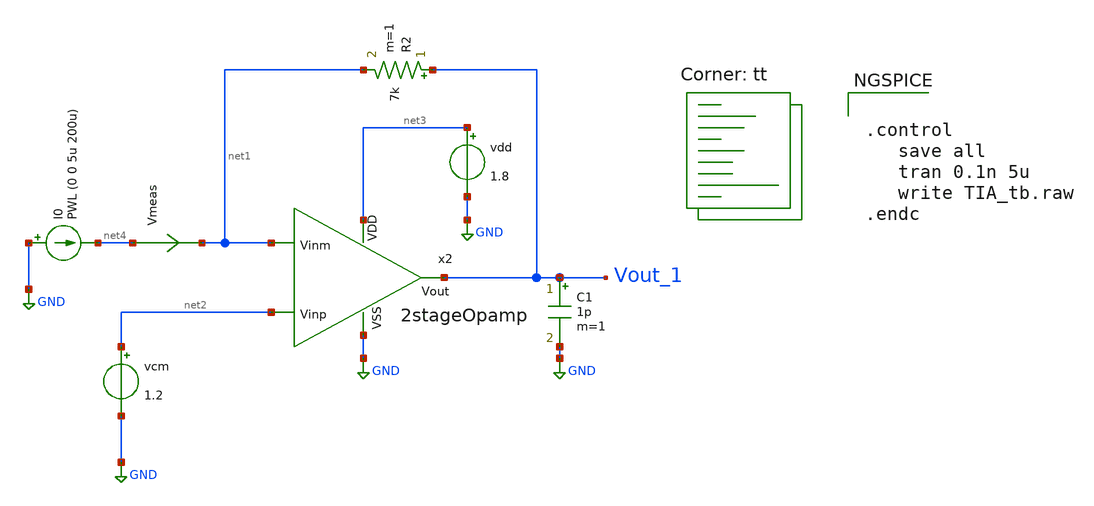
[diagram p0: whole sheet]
** sch_path: xschem/test/xschem/dec24_2stage_tbs/TIA_tb.sch
**.subckt TIA_tb
x2 net3 net1 net2 Vout_1 GND 2stageOpamp
vdd net3 GND 1.8
C1 Vout_1 GND 1p m=1
R2 Vout_1 net1 7k m=1
I0 GND net4 PWL (0 0 5u 200u)
Vmeas net4 net1 0
.save i(vmeas)
vcm net2 GND 1.2
**** begin user architecture code
.lib $::SKYWATER_MODELS/sky130.lib.spice tt


.control
   save all
   tran 0.1n 5u
   write TIA_tb.raw
.endc


**** end user architecture code
**.ends

* expanding   symbol:  amplifiers/dec24/2stageOpamp.sym # of pins=5
** sym_path: amplifiers/dec24/2stageOpamp.sym
** sch_path: amplifiers/dec24/2stageOpamp.sch
.subckt 2stageOpamp VDD Vinm Vinp Vout VSS
*.ipin Vinm
*.ipin Vinp
*.opin Vout
*.ipin VSS
*.ipin VDD
XM8 Vout net1 VSS VSS sky130_fd_pr__nfet_01v8 L=1 W=6 nf=1 ad='int((nf+1)/2) * W/nf * 0.29' as='int((nf+2)/2) * W/nf * 0.29'
+ pd='2*int((nf+1)/2) * (W/nf + 0.29)' ps='2*int((nf+2)/2) * (W/nf + 0.29)' nrd='0.29 / W' nrs='0.29 / W'
+ sa=0 sb=0 sd=0 mult=8 m=8
XM2 Vout Vb1 VDD VDD sky130_fd_pr__pfet_01v8_lvt L=1 W=9 nf=1 ad='int((nf+1)/2) * W/nf * 0.29' as='int((nf+2)/2) * W/nf * 0.29'
+ pd='2*int((nf+1)/2) * (W/nf + 0.29)' ps='2*int((nf+2)/2) * (W/nf + 0.29)' nrd='0.29 / W' nrs='0.29 / W'
+ sa=0 sb=0 sd=0 mult=3 m=3
XM5 net5 Vb3 net6 VSS sky130_fd_pr__nfet_01v8 L=1 W=4 nf=1 ad='int((nf+1)/2) * W/nf * 0.29' as='int((nf+2)/2) * W/nf * 0.29'
+ pd='2*int((nf+1)/2) * (W/nf + 0.29)' ps='2*int((nf+2)/2) * (W/nf + 0.29)' nrd='0.29 / W' nrs='0.29 / W'
+ sa=0 sb=0 sd=0 mult=3 m=3
XM17 net1 Vb3 net7 VSS sky130_fd_pr__nfet_01v8 L=1 W=4 nf=1 ad='int((nf+1)/2) * W/nf * 0.29' as='int((nf+2)/2) * W/nf * 0.29'
+ pd='2*int((nf+1)/2) * (W/nf + 0.29)' ps='2*int((nf+2)/2) * (W/nf + 0.29)' nrd='0.29 / W' nrs='0.29 / W'
+ sa=0 sb=0 sd=0 mult=3 m=3
XM3 net6 net5 VSS VSS sky130_fd_pr__nfet_01v8 L=1 W=8 nf=1 ad='int((nf+1)/2) * W/nf * 0.29' as='int((nf+2)/2) * W/nf * 0.29'
+ pd='2*int((nf+1)/2) * (W/nf + 0.29)' ps='2*int((nf+2)/2) * (W/nf + 0.29)' nrd='0.29 / W' nrs='0.29 / W'
+ sa=0 sb=0 sd=0 mult=1 m=1
XM19 net7 net5 VSS VSS sky130_fd_pr__nfet_01v8 L=1 W=8 nf=1 ad='int((nf+1)/2) * W/nf * 0.29' as='int((nf+2)/2) * W/nf * 0.29'
+ pd='2*int((nf+1)/2) * (W/nf + 0.29)' ps='2*int((nf+2)/2) * (W/nf + 0.29)' nrd='0.29 / W' nrs='0.29 / W'
+ sa=0 sb=0 sd=0 mult=1 m=1
V1 Vb1 GND 1.1
V2 Vb2 GND 0.7
V3 Vb3 GND 0.9
XM11 net8 Vb1 VDD VDD sky130_fd_pr__pfet_01v8_lvt L=1 W=9 nf=1 ad='int((nf+1)/2) * W/nf * 0.29' as='int((nf+2)/2) * W/nf * 0.29'
+ pd='2*int((nf+1)/2) * (W/nf + 0.29)' ps='2*int((nf+2)/2) * (W/nf + 0.29)' nrd='0.29 / W' nrs='0.29 / W'
+ sa=0 sb=0 sd=0 mult=2 m=2
XM1 net6 Vinm net8 VDD sky130_fd_pr__pfet_01v8_lvt L=1 W=8 nf=1 ad='int((nf+1)/2) * W/nf * 0.29' as='int((nf+2)/2) * W/nf * 0.29'
+ pd='2*int((nf+1)/2) * (W/nf + 0.29)' ps='2*int((nf+2)/2) * (W/nf + 0.29)' nrd='0.29 / W' nrs='0.29 / W'
+ sa=0 sb=0 sd=0 mult=3 m=3
XM15 net7 Vinp net8 VDD sky130_fd_pr__pfet_01v8_lvt L=1 W=8 nf=1 ad='int((nf+1)/2) * W/nf * 0.29' as='int((nf+2)/2) * W/nf * 0.29'
+ pd='2*int((nf+1)/2) * (W/nf + 0.29)' ps='2*int((nf+2)/2) * (W/nf + 0.29)' nrd='0.29 / W' nrs='0.29 / W'
+ sa=0 sb=0 sd=0 mult=3 m=3
XM7 net3 Vb1 VDD VDD sky130_fd_pr__pfet_01v8_lvt L=1 W=9 nf=1 ad='int((nf+1)/2) * W/nf * 0.29' as='int((nf+2)/2) * W/nf * 0.29'
+ pd='2*int((nf+1)/2) * (W/nf + 0.29)' ps='2*int((nf+2)/2) * (W/nf + 0.29)' nrd='0.29 / W' nrs='0.29 / W'
+ sa=0 sb=0 sd=0 mult=1 m=1
XM21 net4 Vb1 VDD VDD sky130_fd_pr__pfet_01v8_lvt L=1 W=9 nf=1 ad='int((nf+1)/2) * W/nf * 0.29' as='int((nf+2)/2) * W/nf * 0.29'
+ pd='2*int((nf+1)/2) * (W/nf + 0.29)' ps='2*int((nf+2)/2) * (W/nf + 0.29)' nrd='0.29 / W' nrs='0.29 / W'
+ sa=0 sb=0 sd=0 mult=1 m=1
XM9 net5 Vb2 net3 VDD sky130_fd_pr__pfet_01v8_lvt L=1 W=9 nf=1 ad='int((nf+1)/2) * W/nf * 0.29' as='int((nf+2)/2) * W/nf * 0.29'
+ pd='2*int((nf+1)/2) * (W/nf + 0.29)' ps='2*int((nf+2)/2) * (W/nf + 0.29)' nrd='0.29 / W' nrs='0.29 / W'
+ sa=0 sb=0 sd=0 mult=1 m=1
XM23 net1 Vb2 net4 VDD sky130_fd_pr__pfet_01v8_lvt L=1 W=9 nf=1 ad='int((nf+1)/2) * W/nf * 0.29' as='int((nf+2)/2) * W/nf * 0.29'
+ pd='2*int((nf+1)/2) * (W/nf + 0.29)' ps='2*int((nf+2)/2) * (W/nf + 0.29)' nrd='0.29 / W' nrs='0.29 / W'
+ sa=0 sb=0 sd=0 mult=1 m=1
XC4 net2 Vout sky130_fd_pr__cap_mim_m3_2 W=7 L=7 MF=4 m=4
R4 net1 net2 7k m=1
.ends

.GLOBAL GND
.end
